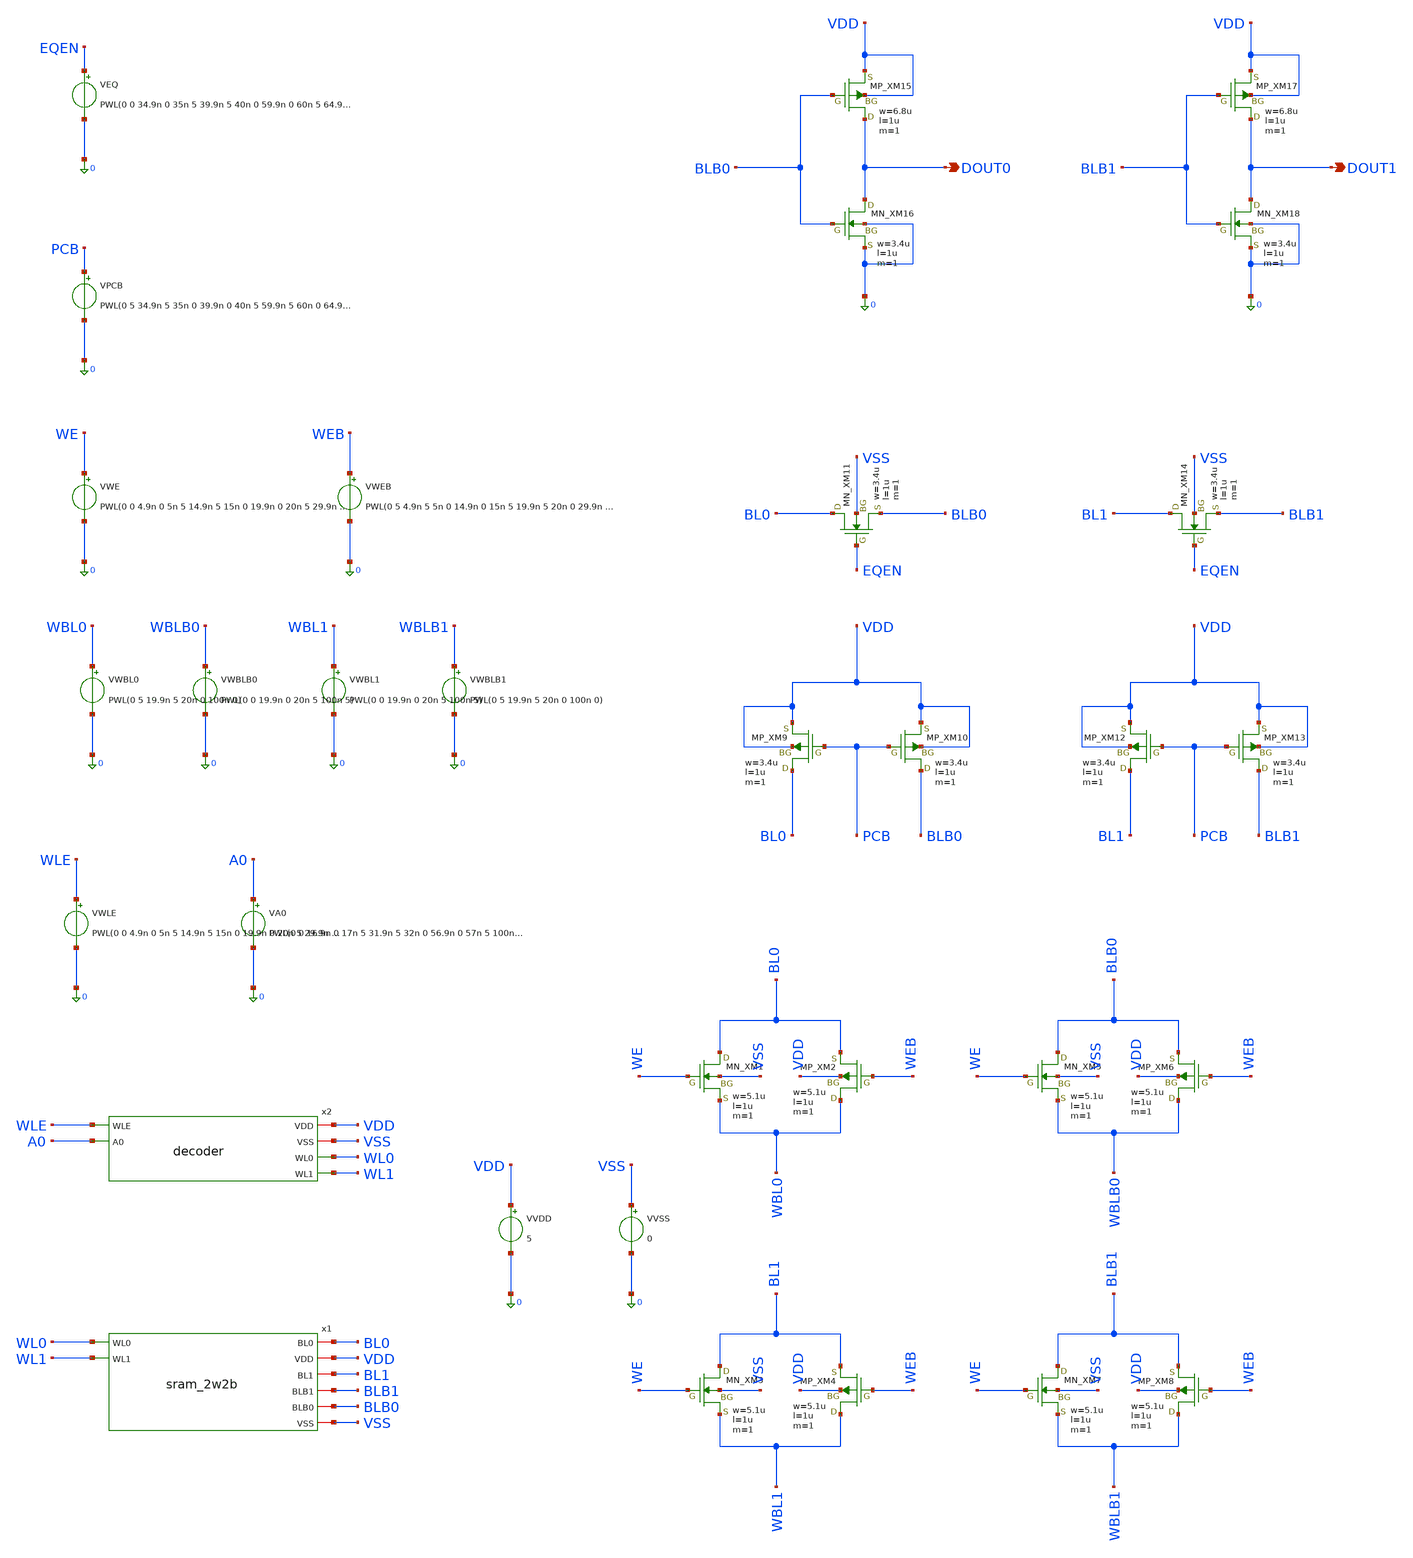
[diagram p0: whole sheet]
** sch_path: array/2word_x_8bit/tb_sram_2w2b_01.sch
**.subckt tb_sram_2w2b_01 DOUT0 DOUT1
*.opin DOUT0
*.opin DOUT1
x1 WL0 BL0 VDD BL1 BLB1 WL1 BLB0 VSS sram_2w2b
VVDD VDD 0 5
XXM1 BL0 WE WBL0 VSS NMOS w=5.1u l=1u nrd=0 nrs=0 m=1
XXM2 WBL0 WEB BL0 VDD PMOS w=5.1u l=1u nrd=0 nrs=0 m=1
XXM5 BLB0 WE WBLB0 VSS NMOS w=5.1u l=1u nrd=0 nrs=0 m=1
XXM6 WBLB0 WEB BLB0 VDD PMOS w=5.1u l=1u nrd=0 nrs=0 m=1
XXM3 BL1 WE WBL1 VSS NMOS w=5.1u l=1u nrd=0 nrs=0 m=1
XXM4 WBL1 WEB BL1 VDD PMOS w=5.1u l=1u nrd=0 nrs=0 m=1
XXM7 BLB1 WE WBLB1 VSS NMOS w=5.1u l=1u nrd=0 nrs=0 m=1
XXM8 WBLB1 WEB BLB1 VDD PMOS w=5.1u l=1u nrd=0 nrs=0 m=1
VWBL0 WBL0 0 PWL(0 5 19.9n 5 20n 0 100n 0)
VWBLB0 WBLB0 0 PWL(0 0 19.9n 0 20n 5 100n 5)
VWBL1 WBL1 0 PWL(0 0 19.9n 0 20n 5 100n 5)
VWBLB1 WBLB1 0 PWL(0 5 19.9n 5 20n 0 100n 0)
VVSS VSS 0 0
VWE WE 0 PWL(0 0 4.9n 0 5n 5 14.9n 5 15n 0 19.9n 0 20n 5 29.9n 5 30n 0 100n 0)
VWEB WEB 0 PWL(0 5 4.9n 5 5n 0 14.9n 0 15n 5 19.9n 5 20n 0 29.9n 0 30n 5 100n 5)
XXM9 BL0 PCB VDD VDD PMOS w=3.4u l=1u nrd=0 nrs=0 m=1
XXM10 BLB0 PCB VDD VDD PMOS w=3.4u l=1u nrd=0 nrs=0 m=1
XXM11 BL0 EQEN BLB0 VSS NMOS w=3.4u l=1u nrd=0 nrs=0 m=1
XXM12 BL1 PCB VDD VDD PMOS w=3.4u l=1u nrd=0 nrs=0 m=1
XXM13 BLB1 PCB VDD VDD PMOS w=3.4u l=1u nrd=0 nrs=0 m=1
XXM14 BL1 EQEN BLB1 VSS NMOS w=3.4u l=1u nrd=0 nrs=0 m=1
XXM15 DOUT0 BLB0 VDD VDD PMOS w=6.8u l=1u nrd=0 nrs=0 m=1
XXM16 DOUT0 BLB0 0 0 NMOS w=3.4u l=1u nrd=0 nrs=0 m=1
XXM17 DOUT1 BLB1 VDD VDD PMOS w=6.8u l=1u nrd=0 nrs=0 m=1
XXM18 DOUT1 BLB1 0 0 NMOS w=3.4u l=1u nrd=0 nrs=0 m=1
VPCB PCB 0 PWL(0 5 34.9n 5 35n 0 39.9n 0 40n 5 59.9n 5 60n 0 64.9n 0 65n 5 100n 5)
VEQ EQEN 0 PWL(0 0 34.9n 0 35n 5 39.9n 5 40n 0 59.9n 0 60n 5 64.9n 5 65n 0 100n 0)
x2 VDD VSS WL0 WLE A0 WL1 decoder
VWLE WLE 0 PWL(0 0 4.9n 0 5n 5 14.9n 5 15n 0 19.9n 0 20n 5 29.9n 5 30n 0 44.9n 0 45n 5 54.9n 5 55n 0
+ 69.9n 0 70n 5 79.9n 5 80n 0 100n 0)
VA0 A0 0 PWL(0 0 16.9n 0 17n 5 31.9n 5 32n 0 56.9n 0 57n 5 100n 5)
**** begin user architecture code
 .include $::LIB/ip62_models


.tran 10p 100n

.meas tran t_read0 TRIG v(wl0) VAL=2.5 RISE=2 TARG v(dout0) VAL=2.5 RISE=1 TD=40n
.meas tran t_read1 TRIG v(wl1) VAL=2.5 RISE=2 TARG v(dout1) VAL=2.5 RISE=1 TD=65n



**** end user architecture code
**.ends
.end
